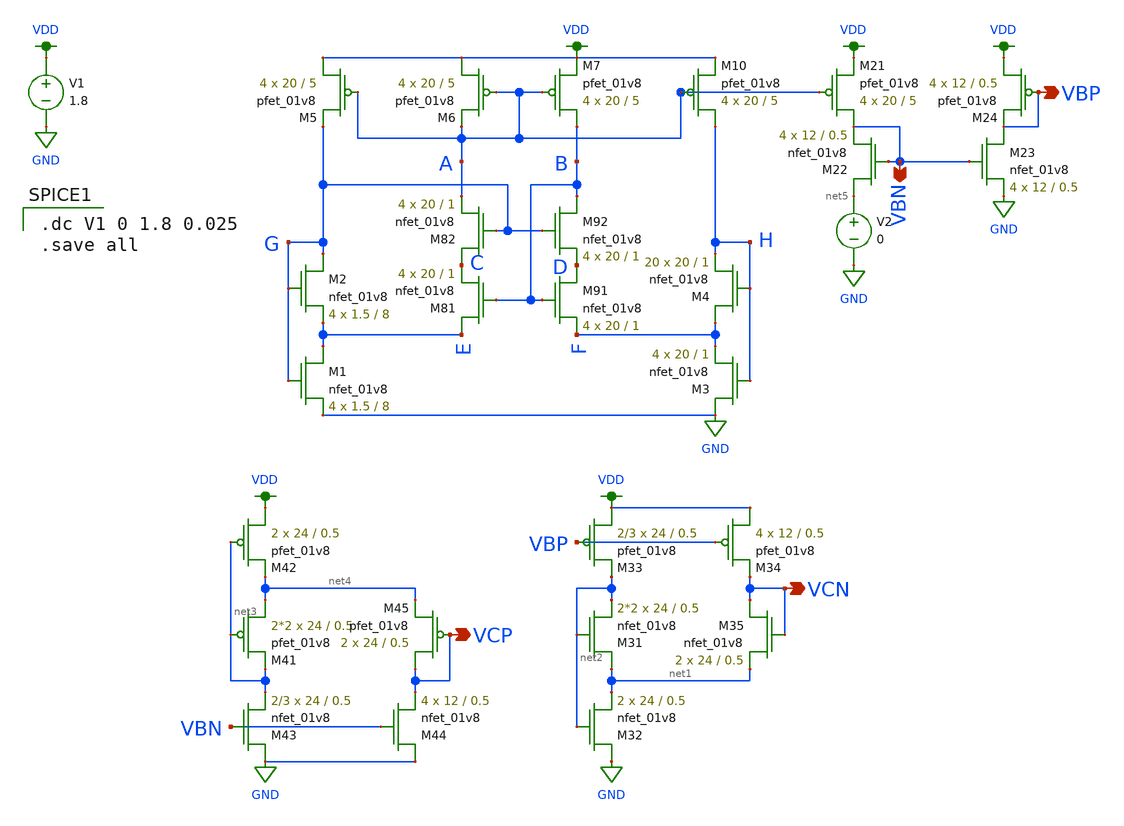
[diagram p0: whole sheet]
** sch_path: miniproject_03/xschem/bias_gen_alt.sch
**.subckt bias_gen_alt VBP VBN VCP VCN
*.opin VBP
*.opin VBN
*.opin VCP
*.opin VCN
V1 VDD GND 1.8
XM10 H A VDD VDD sky130_fd_pr__pfet_01v8 L=5 W=20 nf=1 ad='int((nf+1)/2) * W/nf * 0.29' as='int((nf+2)/2) * W/nf * 0.29'
+ pd='2*int((nf+1)/2) * (W/nf + 0.29)' ps='2*int((nf+2)/2) * (W/nf + 0.29)' nrd='0.29 / W' nrs='0.29 / W'
+ sa=0 sb=0 sd=0 mult=4 m=4
XM82 C G A GND sky130_fd_pr__nfet_01v8 L=1 W=20 nf=1 ad='int((nf+1)/2) * W/nf * 0.29' as='int((nf+2)/2) * W/nf * 0.29'
+ pd='2*int((nf+1)/2) * (W/nf + 0.29)' ps='2*int((nf+2)/2) * (W/nf + 0.29)' nrd='0.29 / W' nrs='0.29 / W'
+ sa=0 sb=0 sd=0 mult=4 m=4
XM92 B G D GND sky130_fd_pr__nfet_01v8 L=1 W=20 nf=1 ad='int((nf+1)/2) * W/nf * 0.29' as='int((nf+2)/2) * W/nf * 0.29'
+ pd='2*int((nf+1)/2) * (W/nf + 0.29)' ps='2*int((nf+2)/2) * (W/nf + 0.29)' nrd='0.29 / W' nrs='0.29 / W'
+ sa=0 sb=0 sd=0 mult=4 m=4
XM91 D B F GND sky130_fd_pr__nfet_01v8 L=1 W=20 nf=1 ad='int((nf+1)/2) * W/nf * 0.29' as='int((nf+2)/2) * W/nf * 0.29'
+ pd='2*int((nf+1)/2) * (W/nf + 0.29)' ps='2*int((nf+2)/2) * (W/nf + 0.29)' nrd='0.29 / W' nrs='0.29 / W'
+ sa=0 sb=0 sd=0 mult=4 m=4
XM81 E B C GND sky130_fd_pr__nfet_01v8 L=1 W=20 nf=1 ad='int((nf+1)/2) * W/nf * 0.29' as='int((nf+2)/2) * W/nf * 0.29'
+ pd='2*int((nf+1)/2) * (W/nf + 0.29)' ps='2*int((nf+2)/2) * (W/nf + 0.29)' nrd='0.29 / W' nrs='0.29 / W'
+ sa=0 sb=0 sd=0 mult=4 m=4
XM1 E G GND GND sky130_fd_pr__nfet_01v8 L=8 W=1.5 nf=1 ad='int((nf+1)/2) * W/nf * 0.29' as='int((nf+2)/2) * W/nf * 0.29'
+ pd='2*int((nf+1)/2) * (W/nf + 0.29)' ps='2*int((nf+2)/2) * (W/nf + 0.29)' nrd='0.29 / W' nrs='0.29 / W'
+ sa=0 sb=0 sd=0 mult=4 m=4
XM2 G G E GND sky130_fd_pr__nfet_01v8 L=8 W=1.5 nf=1 ad='int((nf+1)/2) * W/nf * 0.29' as='int((nf+2)/2) * W/nf * 0.29'
+ pd='2*int((nf+1)/2) * (W/nf + 0.29)' ps='2*int((nf+2)/2) * (W/nf + 0.29)' nrd='0.29 / W' nrs='0.29 / W'
+ sa=0 sb=0 sd=0 mult=4 m=4
XM3 GND H F GND sky130_fd_pr__nfet_01v8 L=1 W=20 nf=1 ad='int((nf+1)/2) * W/nf * 0.29' as='int((nf+2)/2) * W/nf * 0.29'
+ pd='2*int((nf+1)/2) * (W/nf + 0.29)' ps='2*int((nf+2)/2) * (W/nf + 0.29)' nrd='0.29 / W' nrs='0.29 / W'
+ sa=0 sb=0 sd=0 mult=4 m=4
XM4 F H H GND sky130_fd_pr__nfet_01v8 L=1 W=20 nf=1 ad='int((nf+1)/2) * W/nf * 0.29' as='int((nf+2)/2) * W/nf * 0.29'
+ pd='2*int((nf+1)/2) * (W/nf + 0.29)' ps='2*int((nf+2)/2) * (W/nf + 0.29)' nrd='0.29 / W' nrs='0.29 / W'
+ sa=0 sb=0 sd=0 mult=20 m=20
XM22 net5 VBN VBN GND sky130_fd_pr__nfet_01v8 L=0.5 W=12 nf=1 ad='int((nf+1)/2) * W/nf * 0.29' as='int((nf+2)/2) * W/nf * 0.29'
+ pd='2*int((nf+1)/2) * (W/nf + 0.29)' ps='2*int((nf+2)/2) * (W/nf + 0.29)' nrd='0.29 / W' nrs='0.29 / W'
+ sa=0 sb=0 sd=0 mult=4 m=4
XM23 VBP VBN GND GND sky130_fd_pr__nfet_01v8 L=0.5 W=12 nf=1 ad='int((nf+1)/2) * W/nf * 0.29' as='int((nf+2)/2) * W/nf * 0.29'
+ pd='2*int((nf+1)/2) * (W/nf + 0.29)' ps='2*int((nf+2)/2) * (W/nf + 0.29)' nrd='0.29 / W' nrs='0.29 / W'
+ sa=0 sb=0 sd=0 mult=4 m=4
XM24 VDD VBP VBP VDD sky130_fd_pr__pfet_01v8 L=0.5 W=12 nf=1 ad='int((nf+1)/2) * W/nf * 0.29' as='int((nf+2)/2) * W/nf * 0.29'
+ pd='2*int((nf+1)/2) * (W/nf + 0.29)' ps='2*int((nf+2)/2) * (W/nf + 0.29)' nrd='0.29 / W' nrs='0.29 / W'
+ sa=0 sb=0 sd=0 mult=4 m=4
XM31 net1 net2 net2 GND sky130_fd_pr__nfet_01v8 L=0.5 W=24 nf=1 ad='int((nf+1)/2) * W/nf * 0.29' as='int((nf+2)/2) * W/nf * 0.29'
+ pd='2*int((nf+1)/2) * (W/nf + 0.29)' ps='2*int((nf+2)/2) * (W/nf + 0.29)' nrd='0.29 / W' nrs='0.29 / W'
+ sa=0 sb=0 sd=0 mult=2*2 m=2*2
XM33 VDD VBP net2 VDD sky130_fd_pr__pfet_01v8 L=0.5 W=24 nf=1 ad='int((nf+1)/2) * W/nf * 0.29' as='int((nf+2)/2) * W/nf * 0.29'
+ pd='2*int((nf+1)/2) * (W/nf + 0.29)' ps='2*int((nf+2)/2) * (W/nf + 0.29)' nrd='0.29 / W' nrs='0.29 / W'
+ sa=0 sb=0 sd=0 mult=2/3 m=2/3
XM32 GND net2 net1 GND sky130_fd_pr__nfet_01v8 L=0.5 W=24 nf=1 ad='int((nf+1)/2) * W/nf * 0.29' as='int((nf+2)/2) * W/nf * 0.29'
+ pd='2*int((nf+1)/2) * (W/nf + 0.29)' ps='2*int((nf+2)/2) * (W/nf + 0.29)' nrd='0.29 / W' nrs='0.29 / W'
+ sa=0 sb=0 sd=0 mult=2 m=2
XM34 VDD VBP VCN VDD sky130_fd_pr__pfet_01v8 L=0.5 W=12 nf=1 ad='int((nf+1)/2) * W/nf * 0.29' as='int((nf+2)/2) * W/nf * 0.29'
+ pd='2*int((nf+1)/2) * (W/nf + 0.29)' ps='2*int((nf+2)/2) * (W/nf + 0.29)' nrd='0.29 / W' nrs='0.29 / W'
+ sa=0 sb=0 sd=0 mult=4 m=4
XM35 VCN VCN net1 GND sky130_fd_pr__nfet_01v8 L=0.5 W=24 nf=1 ad='int((nf+1)/2) * W/nf * 0.29' as='int((nf+2)/2) * W/nf * 0.29'
+ pd='2*int((nf+1)/2) * (W/nf + 0.29)' ps='2*int((nf+2)/2) * (W/nf + 0.29)' nrd='0.29 / W' nrs='0.29 / W'
+ sa=0 sb=0 sd=0 mult=2 m=2
XM41 net4 net3 net3 VDD sky130_fd_pr__pfet_01v8 L=0.5 W=24 nf=1 ad='int((nf+1)/2) * W/nf * 0.29' as='int((nf+2)/2) * W/nf * 0.29'
+ pd='2*int((nf+1)/2) * (W/nf + 0.29)' ps='2*int((nf+2)/2) * (W/nf + 0.29)' nrd='0.29 / W' nrs='0.29 / W'
+ sa=0 sb=0 sd=0 mult=2*2 m=2*2
XM42 VDD net3 net4 VDD sky130_fd_pr__pfet_01v8 L=0.5 W=24 nf=1 ad='int((nf+1)/2) * W/nf * 0.29' as='int((nf+2)/2) * W/nf * 0.29'
+ pd='2*int((nf+1)/2) * (W/nf + 0.29)' ps='2*int((nf+2)/2) * (W/nf + 0.29)' nrd='0.29 / W' nrs='0.29 / W'
+ sa=0 sb=0 sd=0 mult=2 m=2
XM43 GND VBN net3 GND sky130_fd_pr__nfet_01v8 L=0.5 W=24 nf=1 ad='int((nf+1)/2) * W/nf * 0.29' as='int((nf+2)/2) * W/nf * 0.29'
+ pd='2*int((nf+1)/2) * (W/nf + 0.29)' ps='2*int((nf+2)/2) * (W/nf + 0.29)' nrd='0.29 / W' nrs='0.29 / W'
+ sa=0 sb=0 sd=0 mult=2/3 m=2/3
XM44 GND VBN VCP GND sky130_fd_pr__nfet_01v8 L=0.5 W=12 nf=1 ad='int((nf+1)/2) * W/nf * 0.29' as='int((nf+2)/2) * W/nf * 0.29'
+ pd='2*int((nf+1)/2) * (W/nf + 0.29)' ps='2*int((nf+2)/2) * (W/nf + 0.29)' nrd='0.29 / W' nrs='0.29 / W'
+ sa=0 sb=0 sd=0 mult=4 m=4
XM45 VCP VCP net4 VDD sky130_fd_pr__pfet_01v8 L=0.5 W=24 nf=1 ad='int((nf+1)/2) * W/nf * 0.29' as='int((nf+2)/2) * W/nf * 0.29'
+ pd='2*int((nf+1)/2) * (W/nf + 0.29)' ps='2*int((nf+2)/2) * (W/nf + 0.29)' nrd='0.29 / W' nrs='0.29 / W'
+ sa=0 sb=0 sd=0 mult=2 m=2
V2 net5 GND 0
XM5 VDD A G VDD sky130_fd_pr__pfet_01v8 L=5 W=20 nf=1 ad='int((nf+1)/2) * W/nf * 0.29' as='int((nf+2)/2) * W/nf * 0.29'
+ pd='2*int((nf+1)/2) * (W/nf + 0.29)' ps='2*int((nf+2)/2) * (W/nf + 0.29)' nrd='0.29 / W' nrs='0.29 / W'
+ sa=0 sb=0 sd=0 mult=4 m=4
XM6 VDD A A VDD sky130_fd_pr__pfet_01v8 L=5 W=20 nf=1 ad='int((nf+1)/2) * W/nf * 0.29' as='int((nf+2)/2) * W/nf * 0.29'
+ pd='2*int((nf+1)/2) * (W/nf + 0.29)' ps='2*int((nf+2)/2) * (W/nf + 0.29)' nrd='0.29 / W' nrs='0.29 / W'
+ sa=0 sb=0 sd=0 mult=4 m=4
XM7 B A VDD VDD sky130_fd_pr__pfet_01v8 L=5 W=20 nf=1 ad='int((nf+1)/2) * W/nf * 0.29' as='int((nf+2)/2) * W/nf * 0.29'
+ pd='2*int((nf+1)/2) * (W/nf + 0.29)' ps='2*int((nf+2)/2) * (W/nf + 0.29)' nrd='0.29 / W' nrs='0.29 / W'
+ sa=0 sb=0 sd=0 mult=4 m=4
XM21 VBN A VDD VDD sky130_fd_pr__pfet_01v8 L=5 W=20 nf=1 ad='int((nf+1)/2) * W/nf * 0.29' as='int((nf+2)/2) * W/nf * 0.29'
+ pd='2*int((nf+1)/2) * (W/nf + 0.29)' ps='2*int((nf+2)/2) * (W/nf + 0.29)' nrd='0.29 / W' nrs='0.29 / W'
+ sa=0 sb=0 sd=0 mult=4 m=4
**** begin user architecture code

.dc V1 0 1.8 0.025
.save all


.option wnflag=1
.lib ~/skywater/skywater-pdk/libraries/sky130_fd_pr_ngspice/latest/models/sky130.lib.spice tt

**** end user architecture code
**.ends
.GLOBAL VDD
.GLOBAL GND
.end
